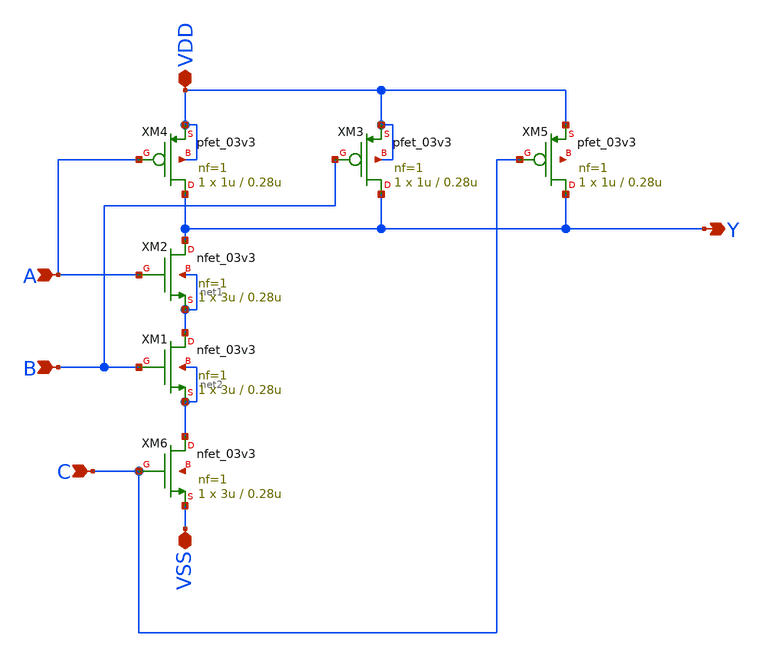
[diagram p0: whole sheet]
** sch_path: team_src/xschem/NAND3_v1.sch
**.subckt NAND3_v1 VSS VDD A Y B C
*.iopin VSS
*.iopin VDD
*.ipin A
*.opin Y
*.ipin B
*.ipin C
XM1 net1 B net2 net2 nfet_03v3 L=0.28u W=3u nf=1 ad='int((nf+1)/2) * W/nf * 0.18u' as='int((nf+2)/2) * W/nf * 0.18u'
+ pd='2*int((nf+1)/2) * (W/nf + 0.18u)' ps='2*int((nf+2)/2) * (W/nf + 0.18u)' nrd='0.18u / W' nrs='0.18u / W'
+ sa=0 sb=0 sd=0 m=1
XM2 Y A net1 net1 nfet_03v3 L=0.28u W=3u nf=1 ad='int((nf+1)/2) * W/nf * 0.18u' as='int((nf+2)/2) * W/nf * 0.18u'
+ pd='2*int((nf+1)/2) * (W/nf + 0.18u)' ps='2*int((nf+2)/2) * (W/nf + 0.18u)' nrd='0.18u / W' nrs='0.18u / W'
+ sa=0 sb=0 sd=0 m=1
XM3 Y B VDD VDD pfet_03v3 L=0.28u W=1u nf=1 ad='int((nf+1)/2) * W/nf * 0.18u' as='int((nf+2)/2) * W/nf * 0.18u'
+ pd='2*int((nf+1)/2) * (W/nf + 0.18u)' ps='2*int((nf+2)/2) * (W/nf + 0.18u)' nrd='0.18u / W' nrs='0.18u / W'
+ sa=0 sb=0 sd=0 m=1
XM4 Y A VDD VDD pfet_03v3 L=0.28u W=1u nf=1 ad='int((nf+1)/2) * W/nf * 0.18u' as='int((nf+2)/2) * W/nf * 0.18u'
+ pd='2*int((nf+1)/2) * (W/nf + 0.18u)' ps='2*int((nf+2)/2) * (W/nf + 0.18u)' nrd='0.18u / W' nrs='0.18u / W'
+ sa=0 sb=0 sd=0 m=1
XM5 Y C VDD net3 pfet_03v3 L=0.28u W=1u nf=1 ad='int((nf+1)/2) * W/nf * 0.18u' as='int((nf+2)/2) * W/nf * 0.18u'
+ pd='2*int((nf+1)/2) * (W/nf + 0.18u)' ps='2*int((nf+2)/2) * (W/nf + 0.18u)' nrd='0.18u / W' nrs='0.18u / W'
+ sa=0 sb=0 sd=0 m=1
XM6 net2 C VSS net4 nfet_03v3 L=0.28u W=3u nf=1 ad='int((nf+1)/2) * W/nf * 0.18u' as='int((nf+2)/2) * W/nf * 0.18u'
+ pd='2*int((nf+1)/2) * (W/nf + 0.18u)' ps='2*int((nf+2)/2) * (W/nf + 0.18u)' nrd='0.18u / W' nrs='0.18u / W'
+ sa=0 sb=0 sd=0 m=1
**.ends
.end
